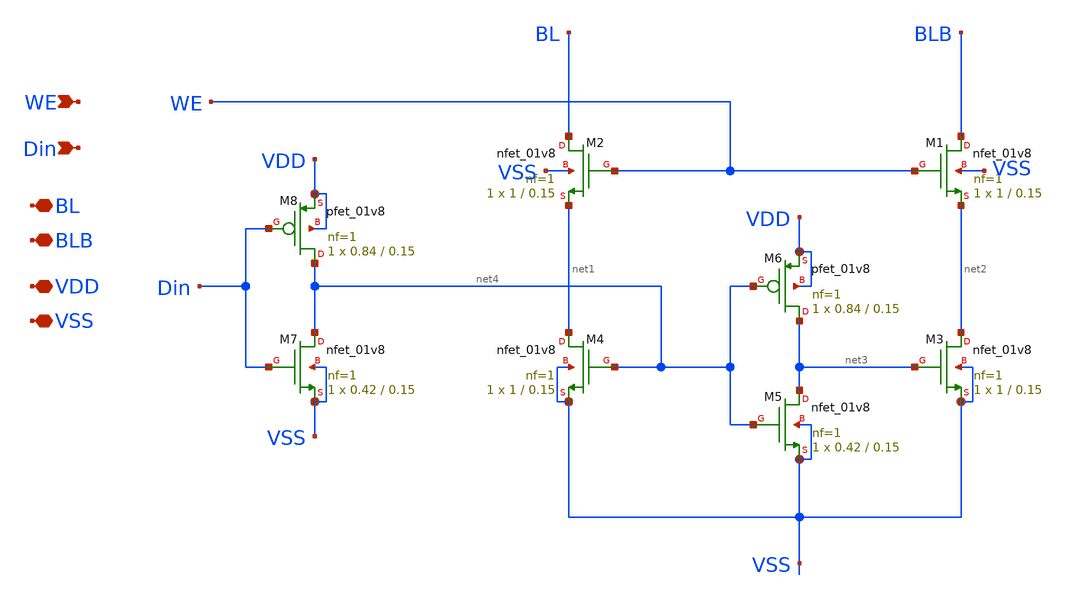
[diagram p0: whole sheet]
** sch_path: xschem/Integrated_bitcell/Write_Driver.sch
**.subckt Write_Driver WE Din BL BLB VDD VSS
*.ipin WE
*.ipin Din
*.iopin BL
*.iopin BLB
*.iopin VDD
*.iopin VSS
XM1 BLB WE net2 VSS sky130_fd_pr__nfet_01v8 L=0.15 W=1 nf=1 ad='int((nf+1)/2) * W/nf * 0.29' as='int((nf+2)/2) * W/nf * 0.29'
+ pd='2*int((nf+1)/2) * (W/nf + 0.29)' ps='2*int((nf+2)/2) * (W/nf + 0.29)' nrd='0.29 / W' nrs='0.29 / W'
+ sa=0 sb=0 sd=0 mult=1 m=1
XM2 BL WE net1 VSS sky130_fd_pr__nfet_01v8 L=0.15 W=1 nf=1 ad='int((nf+1)/2) * W/nf * 0.29' as='int((nf+2)/2) * W/nf * 0.29'
+ pd='2*int((nf+1)/2) * (W/nf + 0.29)' ps='2*int((nf+2)/2) * (W/nf + 0.29)' nrd='0.29 / W' nrs='0.29 / W'
+ sa=0 sb=0 sd=0 mult=1 m=1
XM3 net2 net3 VSS VSS sky130_fd_pr__nfet_01v8 L=0.15 W=1 nf=1 ad='int((nf+1)/2) * W/nf * 0.29' as='int((nf+2)/2) * W/nf * 0.29'
+ pd='2*int((nf+1)/2) * (W/nf + 0.29)' ps='2*int((nf+2)/2) * (W/nf + 0.29)' nrd='0.29 / W' nrs='0.29 / W'
+ sa=0 sb=0 sd=0 mult=1 m=1
XM4 net1 net4 VSS VSS sky130_fd_pr__nfet_01v8 L=0.15 W=1 nf=1 ad='int((nf+1)/2) * W/nf * 0.29' as='int((nf+2)/2) * W/nf * 0.29'
+ pd='2*int((nf+1)/2) * (W/nf + 0.29)' ps='2*int((nf+2)/2) * (W/nf + 0.29)' nrd='0.29 / W' nrs='0.29 / W'
+ sa=0 sb=0 sd=0 mult=1 m=1
XM5 net3 net4 VSS VSS sky130_fd_pr__nfet_01v8 L=0.15 W=0.42 nf=1 ad='int((nf+1)/2) * W/nf * 0.29' as='int((nf+2)/2) * W/nf * 0.29'
+ pd='2*int((nf+1)/2) * (W/nf + 0.29)' ps='2*int((nf+2)/2) * (W/nf + 0.29)' nrd='0.29 / W' nrs='0.29 / W'
+ sa=0 sb=0 sd=0 mult=1 m=1
XM6 net3 net4 VDD VDD sky130_fd_pr__pfet_01v8 L=0.15 W=0.84 nf=1 ad='int((nf+1)/2) * W/nf * 0.29' as='int((nf+2)/2) * W/nf * 0.29'
+ pd='2*int((nf+1)/2) * (W/nf + 0.29)' ps='2*int((nf+2)/2) * (W/nf + 0.29)' nrd='0.29 / W' nrs='0.29 / W'
+ sa=0 sb=0 sd=0 mult=1 m=1
XM7 net4 Din VSS VSS sky130_fd_pr__nfet_01v8 L=0.15 W=0.42 nf=1 ad='int((nf+1)/2) * W/nf * 0.29' as='int((nf+2)/2) * W/nf * 0.29'
+ pd='2*int((nf+1)/2) * (W/nf + 0.29)' ps='2*int((nf+2)/2) * (W/nf + 0.29)' nrd='0.29 / W' nrs='0.29 / W'
+ sa=0 sb=0 sd=0 mult=1 m=1
XM8 net4 Din VDD VDD sky130_fd_pr__pfet_01v8 L=0.15 W=0.84 nf=1 ad='int((nf+1)/2) * W/nf * 0.29' as='int((nf+2)/2) * W/nf * 0.29'
+ pd='2*int((nf+1)/2) * (W/nf + 0.29)' ps='2*int((nf+2)/2) * (W/nf + 0.29)' nrd='0.29 / W' nrs='0.29 / W'
+ sa=0 sb=0 sd=0 mult=1 m=1
**.ends
.end
